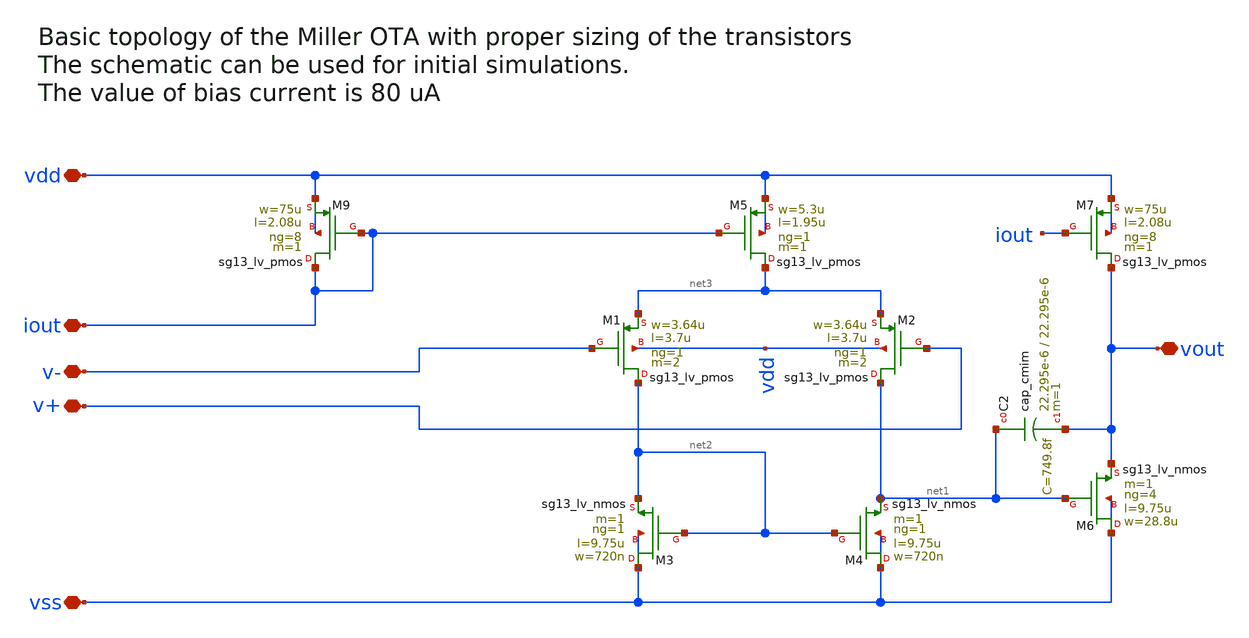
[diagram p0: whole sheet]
** sch_path: tests/data/_corecheck/basic-payload.roundtrip.sch
**.subckt basic-payload.roundtrip v- v+ vss vdd iout vout
*.iopin v-
*.iopin v+
*.iopin vss
*.iopin vdd
*.iopin iout
*.iopin vout
XM4 vss net2 net1 vss sg13_lv_nmos w=720n l=9.75u ng=1 m=1 mm_ok=1
XM3 vss net2 net2 vss sg13_lv_nmos w=720n l=9.75u ng=1 m=1 mm_ok=1
XM1 net2 v- net3 vdd sg13_lv_pmos w=3.64u l=3.7u ng=1 m=2 mm_ok=1
XM2 net1 v+ net3 vdd sg13_lv_pmos w=3.64u l=3.7u ng=1 m=2 mm_ok=1
XM5 net3 iout vdd vdd sg13_lv_pmos w=5.3u l=1.95u ng=1 m=1 mm_ok=0
XM7 vout iout vdd vdd sg13_lv_pmos w=75u l=2.08u ng=8 m=1 mm_ok=0
XM6 vss net1 vout vss sg13_lv_nmos w=28.8u l=9.75u ng=4 m=1 mm_ok=0
XM9 iout iout vdd vdd sg13_lv_pmos w=75u l=2.08u ng=8 m=1 mm_ok=0
XC2 net1 vout cap_cmim w=22.295e-6 l=22.295e-6 m=1 mm_ok=1
**.ends
.end
